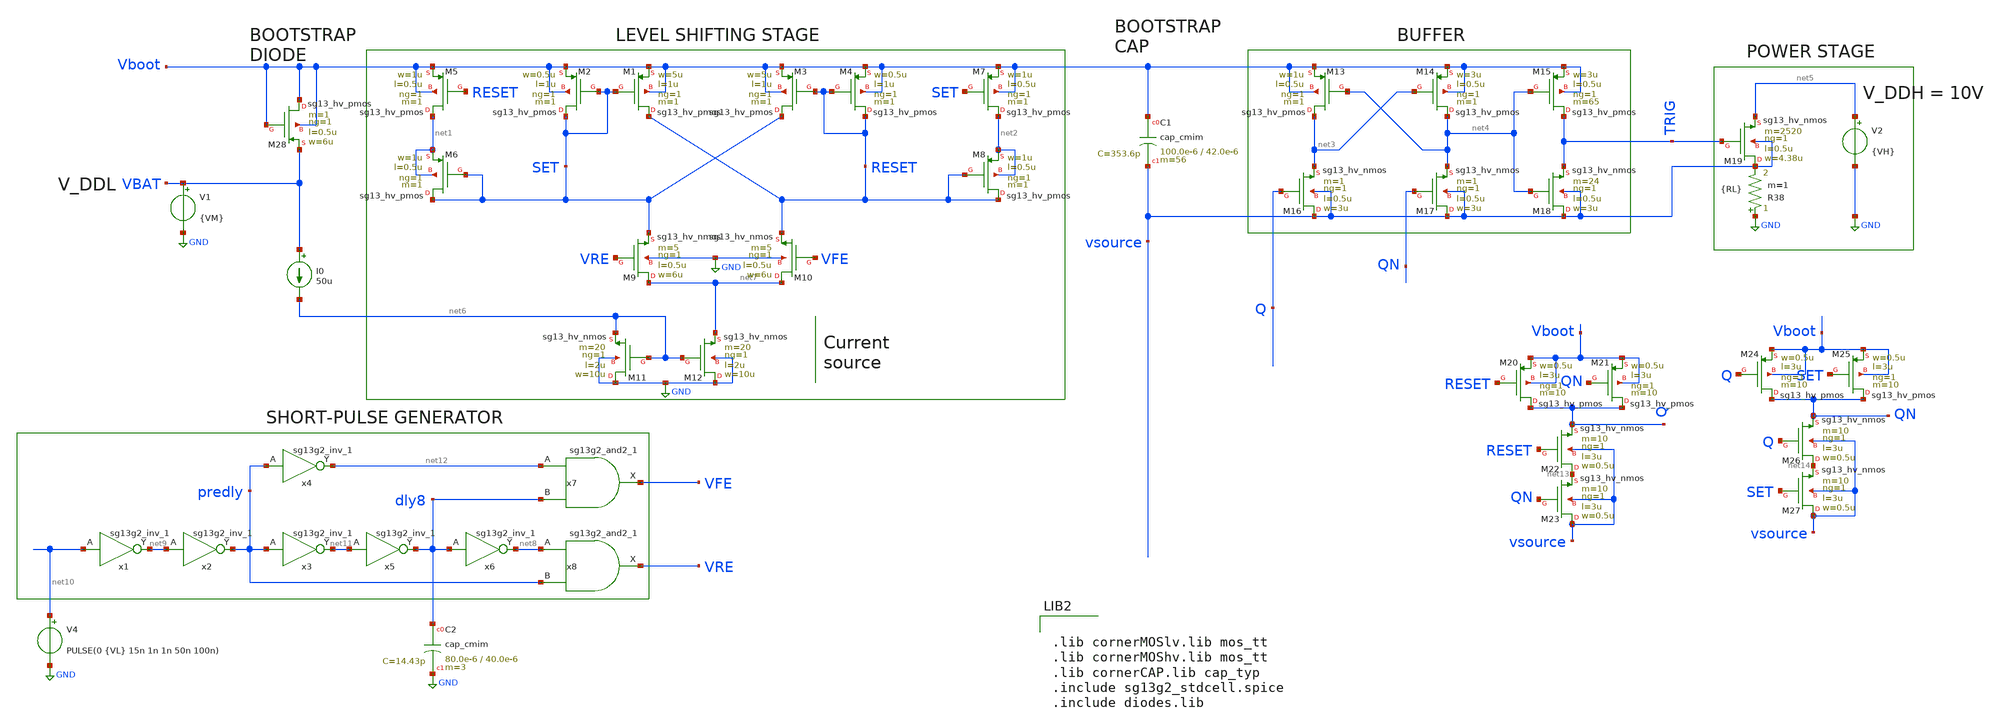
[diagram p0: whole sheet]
** sch_path: xschem/Simulation/LS_boot_ihp_diodo_p.sch
**.subckt LS_boot_ihp_diodo_p
I0 VBAT net6 50u
V4 net10 GND PULSE(0 {VL} 15n 1n 1n 50n 100n)
V1 VBAT GND {VM}
V2 net5 GND {VH}
R38 GND vsource {RL} m=1
XM1 RESET SET Vboot Vboot sg13_hv_pmos w=5u l=1u ng=1 m=1 mm_ok=1
XM2 SET SET Vboot Vboot sg13_hv_pmos w=0.5u l=1u ng=1 m=1 mm_ok=1
XM3 SET RESET Vboot Vboot sg13_hv_pmos w=5u l=1u ng=1 m=1 mm_ok=1
XM4 RESET RESET Vboot Vboot sg13_hv_pmos w=0.5u l=1u ng=1 m=1 mm_ok=1
XM5 net1 RESET Vboot Vboot sg13_hv_pmos w=1u l=0.5u ng=1 m=1 mm_ok=1
XM6 SET SET net1 net1 sg13_hv_pmos w=1u l=0.5u ng=1 m=1 mm_ok=1
XM7 net2 SET Vboot Vboot sg13_hv_pmos w=1u l=0.5u ng=1 m=1 mm_ok=1
XM8 RESET RESET net2 net2 sg13_hv_pmos w=1u l=0.5u ng=1 m=1 mm_ok=1
XM9 net7 VRE SET GND sg13_hv_nmos w=6u l=0.5u ng=1 m=5 mm_ok=1
XM10 net7 VFE RESET GND sg13_hv_nmos w=6u l=0.5u ng=1 m=5 mm_ok=1
XM11 GND net6 net6 GND sg13_hv_nmos w=10u l=2u ng=1 m=20 mm_ok=1
XM12 GND net6 net7 GND sg13_hv_nmos w=10u l=2u ng=1 m=20 mm_ok=1
XM13 net3 net4 Vboot Vboot sg13_hv_pmos w=1u l=0.5u ng=1 m=1 mm_ok=1
XM14 net4 net3 Vboot Vboot sg13_hv_pmos w=3u l=0.5u ng=1 m=1 mm_ok=1
XM15 TRIG net4 Vboot Vboot sg13_hv_pmos w=3u l=0.5u ng=1 m=65 mm_ok=1
XM16 vsource Q net3 vsource sg13_hv_nmos w=3u l=0.5u ng=1 m=1 mm_ok=1
XM17 vsource QN net4 vsource sg13_hv_nmos w=3u l=0.5u ng=1 m=1 mm_ok=1
XM18 vsource net4 TRIG vsource sg13_hv_nmos w=3u l=0.5u ng=1 m=24 mm_ok=1
XM19 vsource TRIG net5 vsource sg13_hv_nmos w=4.38u l=0.5u ng=1 m=2520 mm_ok=1
XM20 Q RESET Vboot Vboot sg13_hv_pmos w=0.5u l=3u ng=1 m=10 mm_ok=1
XM21 Q QN Vboot Vboot sg13_hv_pmos w=0.5u l=3u ng=1 m=10 mm_ok=1
XM22 net13 RESET Q vsource sg13_hv_nmos w=0.5u l=3u ng=1 m=10 mm_ok=1
XM23 vsource QN net13 vsource sg13_hv_nmos w=0.5u l=3u ng=1 m=10 mm_ok=1
XM24 QN Q Vboot Vboot sg13_hv_pmos w=0.5u l=3u ng=1 m=10 mm_ok=1
XM25 QN SET Vboot Vboot sg13_hv_pmos w=0.5u l=3u ng=1 m=10 mm_ok=1
XM26 net14 Q QN vsource sg13_hv_nmos w=0.5u l=3u ng=1 m=10 mm_ok=1
XM27 vsource SET net14 vsource sg13_hv_nmos w=0.5u l=3u ng=1 m=10 mm_ok=1
x1 net9 net10 VDD VSS sg13g2_inv_1
x2 predly net9 VDD VSS sg13g2_inv_1
x3 net11 predly VDD VSS sg13g2_inv_1
x4 net12 predly VDD VSS sg13g2_inv_1
x5 dly8 net11 VDD VSS sg13g2_inv_1
x6 net8 dly8 VDD VSS sg13g2_inv_1
x7 VFE net12 dly8 VDD VSS sg13g2_and2_1
x8 VRE net8 predly VDD VSS sg13g2_and2_1
XC2 dly8 GND cap_cmim w=80.0e-6 l=40.0e-6 m=3 mm_ok=1
XC1 Vboot vsource cap_cmim w=100.0e-6 l=42.0e-6 m=56 mm_ok=1
XM28 Vboot Vboot VBAT Vboot sg13_hv_pmos w=6u l=0.5u ng=1 m=1 mm_ok=1
**** begin user architecture code


VDD VDD GND 1.8
VSS VSS GND 0
.param VH = 10
.param VM = 5
.param VL = 1.8
.param RL = 50

.option maxord=1

.options savecurrents
.control
save all
tran 300n 3000n
plot V(vboot)

*wrdata /foss/designs/Joel/LS_boot_ajustado_sky/datos.txt tran.v(net11) tran.v(vsource) tran.v(TRIG)
.endc




.lib cornerMOSlv.lib mos_tt
.lib cornerMOShv.lib mos_tt
.lib cornerCAP.lib cap_typ
.include sg13g2_stdcell.spice
.include diodes.lib


**** end user architecture code
**.ends

* expanding   symbol:  sg13g2_stdcells/sg13g2_inv_1.sym # of pins=2
** sym_path: sg13g2_stdcells/sg13g2_inv_1.sym
** sch_path: sg13g2_stdcells/sg13g2_inv_1.sch
.subckt sg13g2_inv_1 Y A VDD VSS
*.opin Y
*.ipin A
*.iopin VDD
*.iopin VSS
XM1 Y A VSS VSS sg13_lv_nmos w=740.00n l=130.00n ng=1 m=1 mm_ok=1
XM2 Y A VDD VDD sg13_lv_pmos w=1.12u l=130.00n ng=1 m=1 mm_ok=1
.ends


* expanding   symbol:  sg13g2_stdcells/sg13g2_and2_1.sym # of pins=3
** sym_path: sg13g2_stdcells/sg13g2_and2_1.sym
** sch_path: sg13g2_stdcells/sg13g2_and2_1.sch
.subckt sg13g2_and2_1 X A B VDD VSS
*.ipin A
*.ipin B
*.opin X
*.iopin VDD
*.iopin VSS
XM1 net1 A net2 VSS sg13_lv_nmos w=640.00n l=130.00n ng=1 m=1 mm_ok=1
XM2 net2 B VSS VSS sg13_lv_nmos w=640.00n l=130.00n ng=1 m=1 mm_ok=1
XM3 X net1 VSS VSS sg13_lv_nmos w=740.00n l=130.00n ng=1 m=1 mm_ok=1
XM4 net1 B VDD VDD sg13_lv_pmos w=840.00n l=130.00n ng=1 m=1 mm_ok=1
XM5 net1 A VDD VDD sg13_lv_pmos w=840.00n l=130.00n ng=1 m=1 mm_ok=1
XM6 X net1 VDD VDD sg13_lv_pmos w=1.12u l=130.00n ng=1 m=1 mm_ok=1
.ends

.GLOBAL GND
.end
